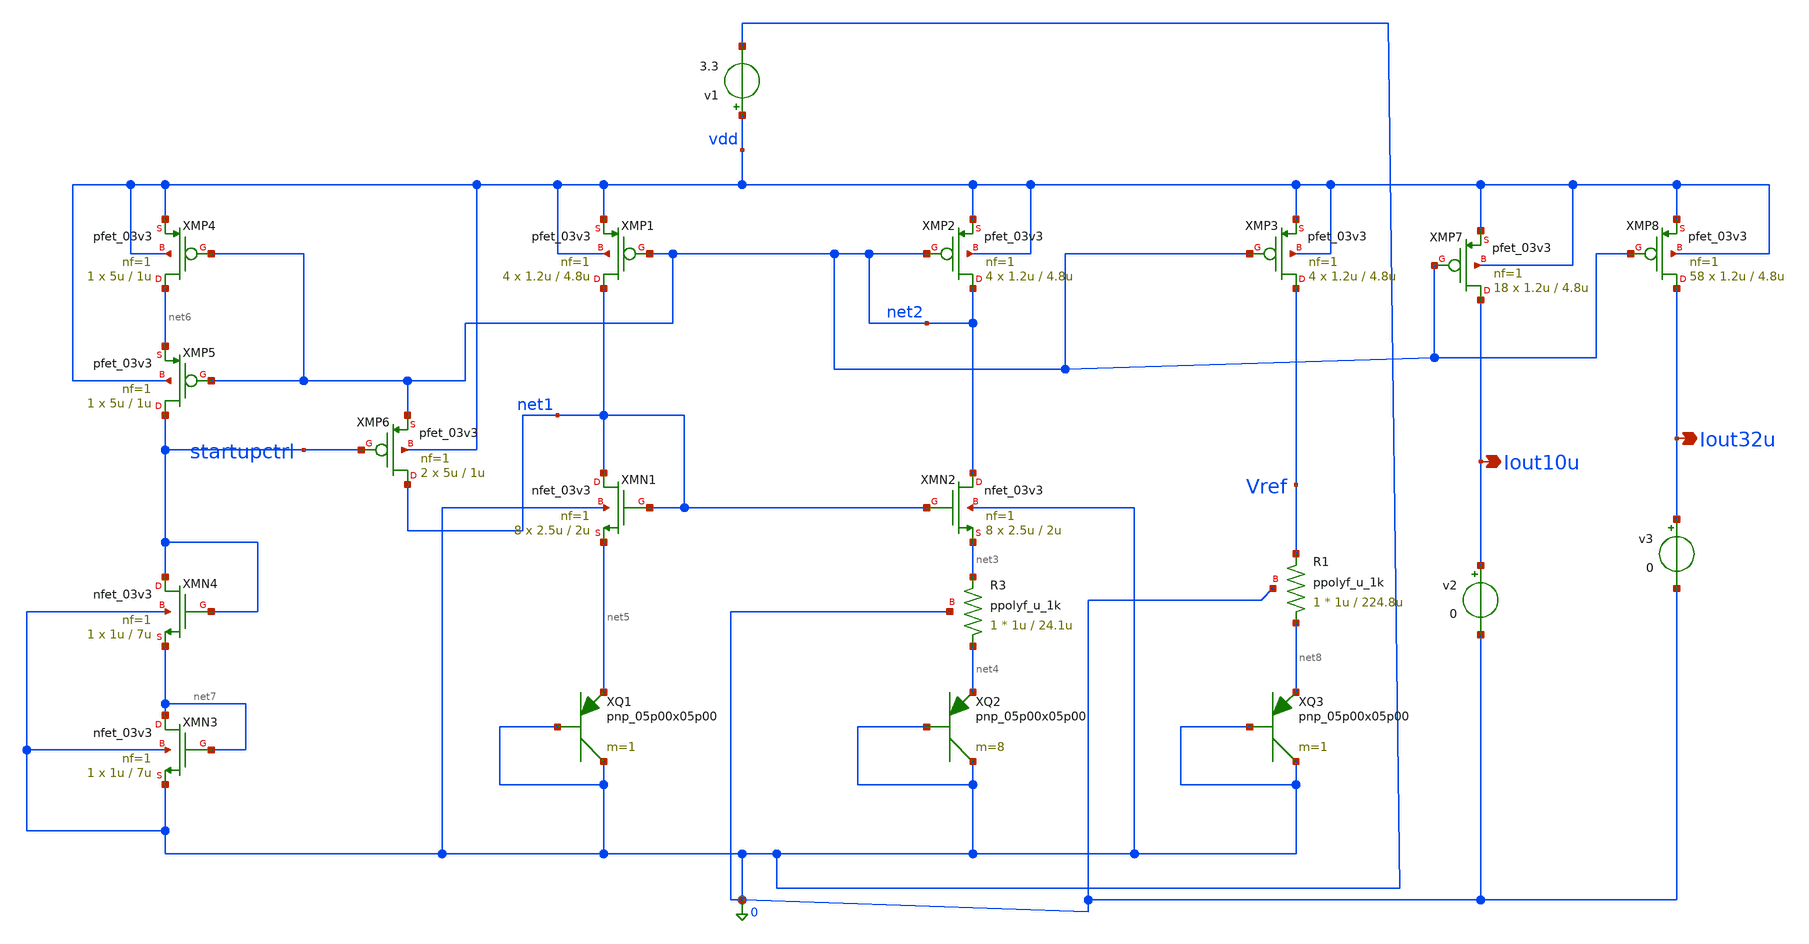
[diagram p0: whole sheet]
** sch_path: schematics/bandgap_3p3.sch
**.subckt bandgap_3p3 Iout10u Iout32u
*.opin Iout10u
*.opin Iout32u
XMP1 net1 net2 vdd vdd pfet_03v3 L=4.8u W=1.2u nf=1 ad='int((nf+1)/2) * W/nf * 0.18u' as='int((nf+2)/2) * W/nf * 0.18u'
+ pd='2*int((nf+1)/2) * (W/nf + 0.18u)' ps='2*int((nf+2)/2) * (W/nf + 0.18u)' nrd='0.18u / W' nrs='0.18u / W'
+ sa=0 sb=0 sd=0 m=4
XMP2 net2 net2 vdd vdd pfet_03v3 L=4.8u W=1.2u nf=1 ad='int((nf+1)/2) * W/nf * 0.18u' as='int((nf+2)/2) * W/nf * 0.18u'
+ pd='2*int((nf+1)/2) * (W/nf + 0.18u)' ps='2*int((nf+2)/2) * (W/nf + 0.18u)' nrd='0.18u / W' nrs='0.18u / W'
+ sa=0 sb=0 sd=0 m=4
XMN1 net1 net1 net5 0 nfet_03v3 L=2u W=2.5u nf=1 ad='int((nf+1)/2) * W/nf * 0.18u' as='int((nf+2)/2) * W/nf * 0.18u'
+ pd='2*int((nf+1)/2) * (W/nf + 0.18u)' ps='2*int((nf+2)/2) * (W/nf + 0.18u)' nrd='0.18u / W' nrs='0.18u / W'
+ sa=0 sb=0 sd=0 m=8
XMN2 net2 net1 net3 0 nfet_03v3 L=2u W=2.5u nf=1 ad='int((nf+1)/2) * W/nf * 0.18u' as='int((nf+2)/2) * W/nf * 0.18u'
+ pd='2*int((nf+1)/2) * (W/nf + 0.18u)' ps='2*int((nf+2)/2) * (W/nf + 0.18u)' nrd='0.18u / W' nrs='0.18u / W'
+ sa=0 sb=0 sd=0 m=8
XMN3 net7 net7 0 0 nfet_03v3 L=7u W=1u nf=1 ad='int((nf+1)/2) * W/nf * 0.18u' as='int((nf+2)/2) * W/nf * 0.18u'
+ pd='2*int((nf+1)/2) * (W/nf + 0.18u)' ps='2*int((nf+2)/2) * (W/nf + 0.18u)' nrd='0.18u / W' nrs='0.18u / W'
+ sa=0 sb=0 sd=0 m=1
XMP3 Vref net2 vdd vdd pfet_03v3 L=4.8u W=1.2u nf=1 ad='int((nf+1)/2) * W/nf * 0.18u' as='int((nf+2)/2) * W/nf * 0.18u'
+ pd='2*int((nf+1)/2) * (W/nf + 0.18u)' ps='2*int((nf+2)/2) * (W/nf + 0.18u)' nrd='0.18u / W' nrs='0.18u / W'
+ sa=0 sb=0 sd=0 m=4
XQ1 0 0 net5 pnp_05p00x05p00 m=1 par=1
XQ2 0 0 net4 pnp_05p00x05p00 m=8 par=8
XQ3 0 0 net8 pnp_05p00x05p00 m=1 par=1
XMP4 net6 net2 vdd vdd pfet_03v3 L=1u W=5u nf=1 ad='int((nf+1)/2) * W/nf * 0.18u' as='int((nf+2)/2) * W/nf * 0.18u'
+ pd='2*int((nf+1)/2) * (W/nf + 0.18u)' ps='2*int((nf+2)/2) * (W/nf + 0.18u)' nrd='0.18u / W' nrs='0.18u / W'
+ sa=0 sb=0 sd=0 m=1
XMP5 startupctrl net2 net6 vdd pfet_03v3 L=1u W=5u nf=1 ad='int((nf+1)/2) * W/nf * 0.18u' as='int((nf+2)/2) * W/nf * 0.18u'
+ pd='2*int((nf+1)/2) * (W/nf + 0.18u)' ps='2*int((nf+2)/2) * (W/nf + 0.18u)' nrd='0.18u / W' nrs='0.18u / W'
+ sa=0 sb=0 sd=0 m=1
XMN4 startupctrl startupctrl net7 0 nfet_03v3 L=7u W=1u nf=1 ad='int((nf+1)/2) * W/nf * 0.18u' as='int((nf+2)/2) * W/nf * 0.18u'
+ pd='2*int((nf+1)/2) * (W/nf + 0.18u)' ps='2*int((nf+2)/2) * (W/nf + 0.18u)' nrd='0.18u / W' nrs='0.18u / W'
+ sa=0 sb=0 sd=0 m=1
XMP6 net1 startupctrl net2 vdd pfet_03v3 L=1u W=5u nf=1 ad='int((nf+1)/2) * W/nf * 0.18u' as='int((nf+2)/2) * W/nf * 0.18u'
+ pd='2*int((nf+1)/2) * (W/nf + 0.18u)' ps='2*int((nf+2)/2) * (W/nf + 0.18u)' nrd='0.18u / W' nrs='0.18u / W'
+ sa=0 sb=0 sd=0 m=2
v1 vdd 0 3.3
XR3 net4 net3 0 ppolyf_u_1k r_width=1u r_length=24.1u m=1
XR1 net8 Vref 0 ppolyf_u_1k r_width=1u r_length=224.8u m=1
XMP7 Iout10u net2 vdd vdd pfet_03v3 L=4.8u W=1.2u nf=1 ad='int((nf+1)/2) * W/nf * 0.18u' as='int((nf+2)/2) * W/nf * 0.18u'
+ pd='2*int((nf+1)/2) * (W/nf + 0.18u)' ps='2*int((nf+2)/2) * (W/nf + 0.18u)' nrd='0.18u / W' nrs='0.18u / W'
+ sa=0 sb=0 sd=0 m=18
XMP8 Iout32u net2 vdd vdd pfet_03v3 L=4.8u W=1.2u nf=1 ad='int((nf+1)/2) * W/nf * 0.18u' as='int((nf+2)/2) * W/nf * 0.18u'
+ pd='2*int((nf+1)/2) * (W/nf + 0.18u)' ps='2*int((nf+2)/2) * (W/nf + 0.18u)' nrd='0.18u / W' nrs='0.18u / W'
+ sa=0 sb=0 sd=0 m=58
v2 Iout10u 0 0
v3 Iout32u 0 0
**** begin user architecture code

************************************************
* GF180 MODEL FILES
************************************************
.include /foss/pdks/gf180mcuD/libs.tech/ngspice/design.ngspice
.lib /foss/pdks/gf180mcuD/libs.tech/ngspice/sm141064.ngspice typical
.lib /foss/pdks/gf180mcuD/libs.tech/ngspice/sm141064.ngspice res_typical
.lib /foss/pdks/gf180mcuD/libs.tech/ngspice/sm141064.ngspice moscap_typical
.lib /foss/pdks/gf180mcuD/libs.tech/ngspice/sm141064.ngspice bjt_typical

.control
op

show all
.endc

**** end user architecture code
**.ends
.end
